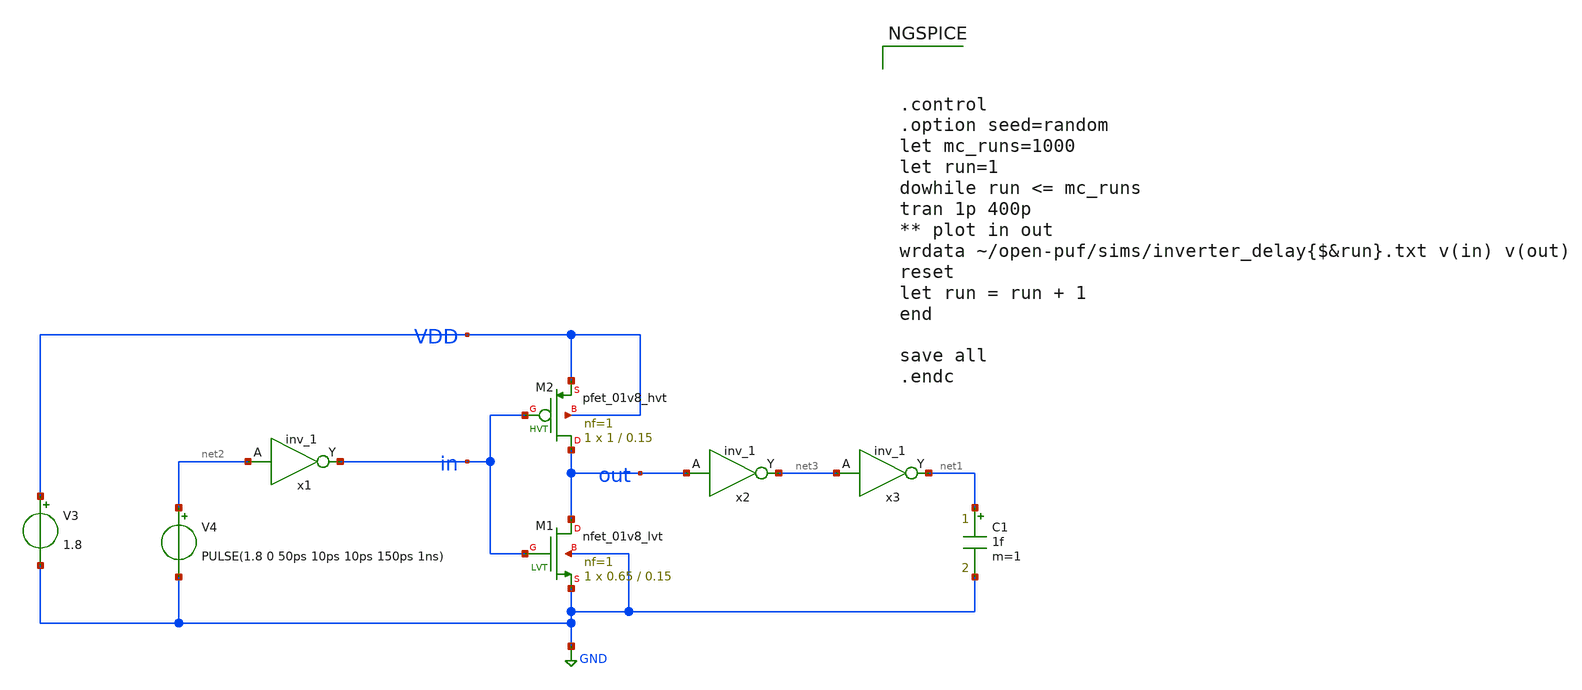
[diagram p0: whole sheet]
** sch_path: design/inverter_delay.sch
**.subckt inverter_delay
C1 net1 GND 1f m=1
XM1 out in GND GND sky130_fd_pr__nfet_01v8_lvt L=0.15 W=0.65 nf=1 ad='int((nf+1)/2) * W/nf * 0.29' as='int((nf+2)/2) * W/nf * 0.29'
+ pd='2*int((nf+1)/2) * (W/nf + 0.29)' ps='2*int((nf+2)/2) * (W/nf + 0.29)' nrd='0.29 / W' nrs='0.29 / W'
+ sa=0 sb=0 sd=0 mult=1 m=1
XM2 out in VDD VDD sky130_fd_pr__pfet_01v8_hvt L=0.15 W=1 nf=1 ad='int((nf+1)/2) * W/nf * 0.29' as='int((nf+2)/2) * W/nf * 0.29'
+ pd='2*int((nf+1)/2) * (W/nf + 0.29)' ps='2*int((nf+2)/2) * (W/nf + 0.29)' nrd='0.29 / W' nrs='0.29 / W'
+ sa=0 sb=0 sd=0 mult=1 m=1
V3 VDD GND 1.8
V4 net2 GND PULSE(1.8 0 50ps 10ps 10ps 150ps 1ns)
x1 net2 0 0 VDD VDD in sky130_fd_sc_hd__inv_1
x2 out 0 0 VDD VDD net3 sky130_fd_sc_hd__inv_1
x3 net3 0 0 VDD VDD net1 sky130_fd_sc_hd__inv_1
**** begin user architecture code

** opencircuitdesign pdks install
.lib $::SKYWATER_MODELS/sky130.lib.spice tt_mm
.include $::SKYWATER_STDCELLS/sky130_fd_sc_hd.spice





.control
.option seed=random
let mc_runs=1000
let run=1
dowhile run <= mc_runs
tran 1p 400p
** plot in out
wrdata ~/open-puf/sims/inverter_delay{$&run}.txt v(in) v(out)
reset
let run = run + 1
end

save all
.endc


**** end user architecture code
**.ends
.GLOBAL GND
.end
